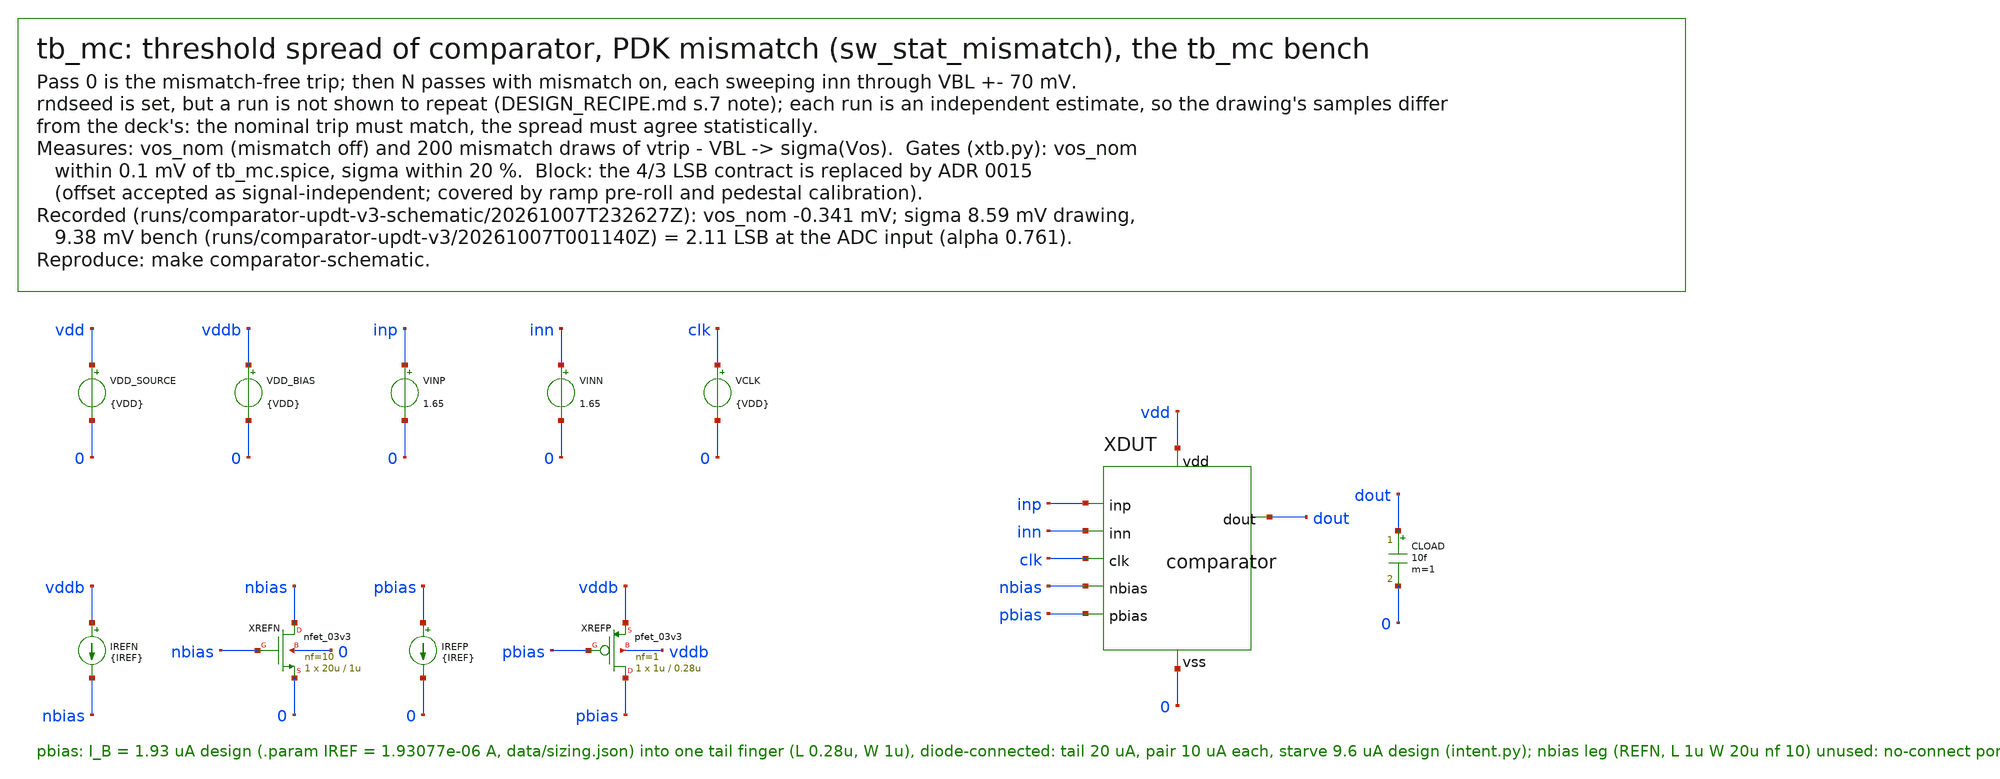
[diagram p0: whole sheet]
** sch_path: mixed_signal/comparator/tb_mc.sch
**.subckt tb_mc
VDD_SOURCE vdd 0 {VDD}
VDD_BIAS vddb 0 {VDD}
VINP inp 0 1.65
VINN inn 0 1.65
VCLK clk 0 {VDD}
IREFN vddb nbias {IREF}
XREFN nbias nbias 0 0 nfet_03v3 L=1u W=20u nf=10 ad='int((nf+1)/2) * W/nf * 0.18u' as='int((nf+2)/2) * W/nf * 0.18u'
+ pd='2*int((nf+1)/2) * (W/nf + 0.18u)' ps='2*int((nf+2)/2) * (W/nf + 0.18u)' nrd='0.18u / W' nrs='0.18u / W'
+ sa=0 sb=0 sd=0 m=1
IREFP pbias 0 {IREF}
XREFP pbias pbias vddb vddb pfet_03v3 L=0.28u W=1u nf=1 ad='int((nf+1)/2) * W/nf * 0.18u' as='int((nf+2)/2) * W/nf * 0.18u'
+ pd='2*int((nf+1)/2) * (W/nf + 0.18u)' ps='2*int((nf+2)/2) * (W/nf + 0.18u)' nrd='0.18u / W' nrs='0.18u / W'
+ sa=0 sb=0 sd=0 m=1
XDUT inp inn dout clk vdd 0 nbias pbias comparator
CLOAD dout 0 10f m=1
**** begin user architecture code

.include /foss/pdks/gf180mcuD/libs.tech/ngspice/design.ngspice
.lib /foss/pdks/gf180mcuD/libs.tech/ngspice/sm141064.ngspice typical
.param sw_stat_mismatch=1
.param VDD=3.3
.param IREF=1.93077e-06   $ data/sizing.json iref: ideal current into one tail finger
.temp 27
.csparam cs_n=200
.control
set rndseed=20261006
let k = 0
alterparam sw_stat_mismatch=0
reset
dc vinn 1.58 1.72 0.0002
meas dc vtrip when v(dout)=1.65 fall=1
let vos_nom = vtrip - 1.65
print vos_nom
alterparam sw_stat_mismatch=1
while k < $&cs_n
  reset
  dc vinn 1.58 1.72 0.0002
  meas dc vtrip when v(dout)=1.65 fall=1
  let vos_k = vtrip - 1.65
  print vos_k
  let k = k + 1
end
quit
.endc

**** end user architecture code
**.ends

* expanding   symbol:  comparator.sym # of pins=8
** sym_path: mixed_signal/comparator/comparator.sym
** sch_path: mixed_signal/comparator/comparator.sch
.subckt comparator inp inn dout clk vdd vss nbias pbias
*.iopin vdd
*.iopin vss
*.ipin pbias
*.ipin inp
*.ipin inn
*.opin dout
*.ipin clk
*.ipin nbias
XTAIL tail pbias vdd vdd pfet_03v3 L=0.28u W=11u nf=11 ad='int((nf+1)/2) * W/nf * 0.18u' as='int((nf+2)/2) * W/nf * 0.18u'
+ pd='2*int((nf+1)/2) * (W/nf + 0.18u)' ps='2*int((nf+2)/2) * (W/nf + 0.18u)' nrd='0.18u / W' nrs='0.18u / W'
+ sa=0 sb=0 sd=0 m=1
XINP left inp tail vdd pfet_03v3 L=0.32u W=12u nf=12 ad='int((nf+1)/2) * W/nf * 0.18u' as='int((nf+2)/2) * W/nf * 0.18u'
+ pd='2*int((nf+1)/2) * (W/nf + 0.18u)' ps='2*int((nf+2)/2) * (W/nf + 0.18u)' nrd='0.18u / W' nrs='0.18u / W'
+ sa=0 sb=0 sd=0 m=1
XINN outa inn tail vdd pfet_03v3 L=0.32u W=12u nf=12 ad='int((nf+1)/2) * W/nf * 0.18u' as='int((nf+2)/2) * W/nf * 0.18u'
+ pd='2*int((nf+1)/2) * (W/nf + 0.18u)' ps='2*int((nf+2)/2) * (W/nf + 0.18u)' nrd='0.18u / W' nrs='0.18u / W'
+ sa=0 sb=0 sd=0 m=1
XLOADD left left vss vss nfet_03v3 L=0.36u W=0.5u nf=1 ad='int((nf+1)/2) * W/nf * 0.18u' as='int((nf+2)/2) * W/nf * 0.18u'
+ pd='2*int((nf+1)/2) * (W/nf + 0.18u)' ps='2*int((nf+2)/2) * (W/nf + 0.18u)' nrd='0.18u / W' nrs='0.18u / W'
+ sa=0 sb=0 sd=0 m=1
XLOADM outa left vss vss nfet_03v3 L=0.36u W=0.5u nf=1 ad='int((nf+1)/2) * W/nf * 0.18u' as='int((nf+2)/2) * W/nf * 0.18u'
+ pd='2*int((nf+1)/2) * (W/nf + 0.18u)' ps='2*int((nf+2)/2) * (W/nf + 0.18u)' nrd='0.18u / W' nrs='0.18u / W'
+ sa=0 sb=0 sd=0 m=1
XBST bst pbias vdd vdd pfet_03v3 L=0.28u W=5u nf=5 ad='int((nf+1)/2) * W/nf * 0.18u' as='int((nf+2)/2) * W/nf * 0.18u'
+ pd='2*int((nf+1)/2) * (W/nf + 0.18u)' ps='2*int((nf+2)/2) * (W/nf + 0.18u)' nrd='0.18u / W' nrs='0.18u / W'
+ sa=0 sb=0 sd=0 m=1
XBUF2 outb outa bst vdd pfet_03v3 L=0.36u W=1u nf=1 ad='int((nf+1)/2) * W/nf * 0.18u' as='int((nf+2)/2) * W/nf * 0.18u'
+ pd='2*int((nf+1)/2) * (W/nf + 0.18u)' ps='2*int((nf+2)/2) * (W/nf + 0.18u)' nrd='0.18u / W' nrs='0.18u / W'
+ sa=0 sb=0 sd=0 m=1
XBUF1 outb outa vss vss nfet_03v3 L=0.36u W=0.5u nf=1 ad='int((nf+1)/2) * W/nf * 0.18u' as='int((nf+2)/2) * W/nf * 0.18u'
+ pd='2*int((nf+1)/2) * (W/nf + 0.18u)' ps='2*int((nf+2)/2) * (W/nf + 0.18u)' nrd='0.18u / W' nrs='0.18u / W'
+ sa=0 sb=0 sd=0 m=1
XBUF4 dout outb vdd vdd pfet_03v3 L=0.36u W=1u nf=1 ad='int((nf+1)/2) * W/nf * 0.18u' as='int((nf+2)/2) * W/nf * 0.18u'
+ pd='2*int((nf+1)/2) * (W/nf + 0.18u)' ps='2*int((nf+2)/2) * (W/nf + 0.18u)' nrd='0.18u / W' nrs='0.18u / W'
+ sa=0 sb=0 sd=0 m=1
XBUF3 dout outb vss vss nfet_03v3 L=0.36u W=0.5u nf=1 ad='int((nf+1)/2) * W/nf * 0.18u' as='int((nf+2)/2) * W/nf * 0.18u'
+ pd='2*int((nf+1)/2) * (W/nf + 0.18u)' ps='2*int((nf+2)/2) * (W/nf + 0.18u)' nrd='0.18u / W' nrs='0.18u / W'
+ sa=0 sb=0 sd=0 m=1
.ends

.end
